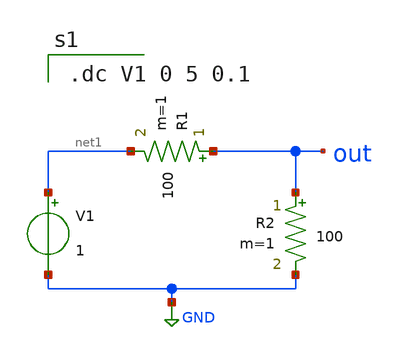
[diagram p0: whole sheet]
** sch_path: tutorial/xschem_1/voltage-divider.sch
**.subckt voltage-divider
V1 net1 GND 1
R2 out GND 100 m=1
R1 out net1 100 m=1
**** begin user architecture code

.dc V1 0 5 0.1

**** end user architecture code
**.ends
.GLOBAL GND
.end
